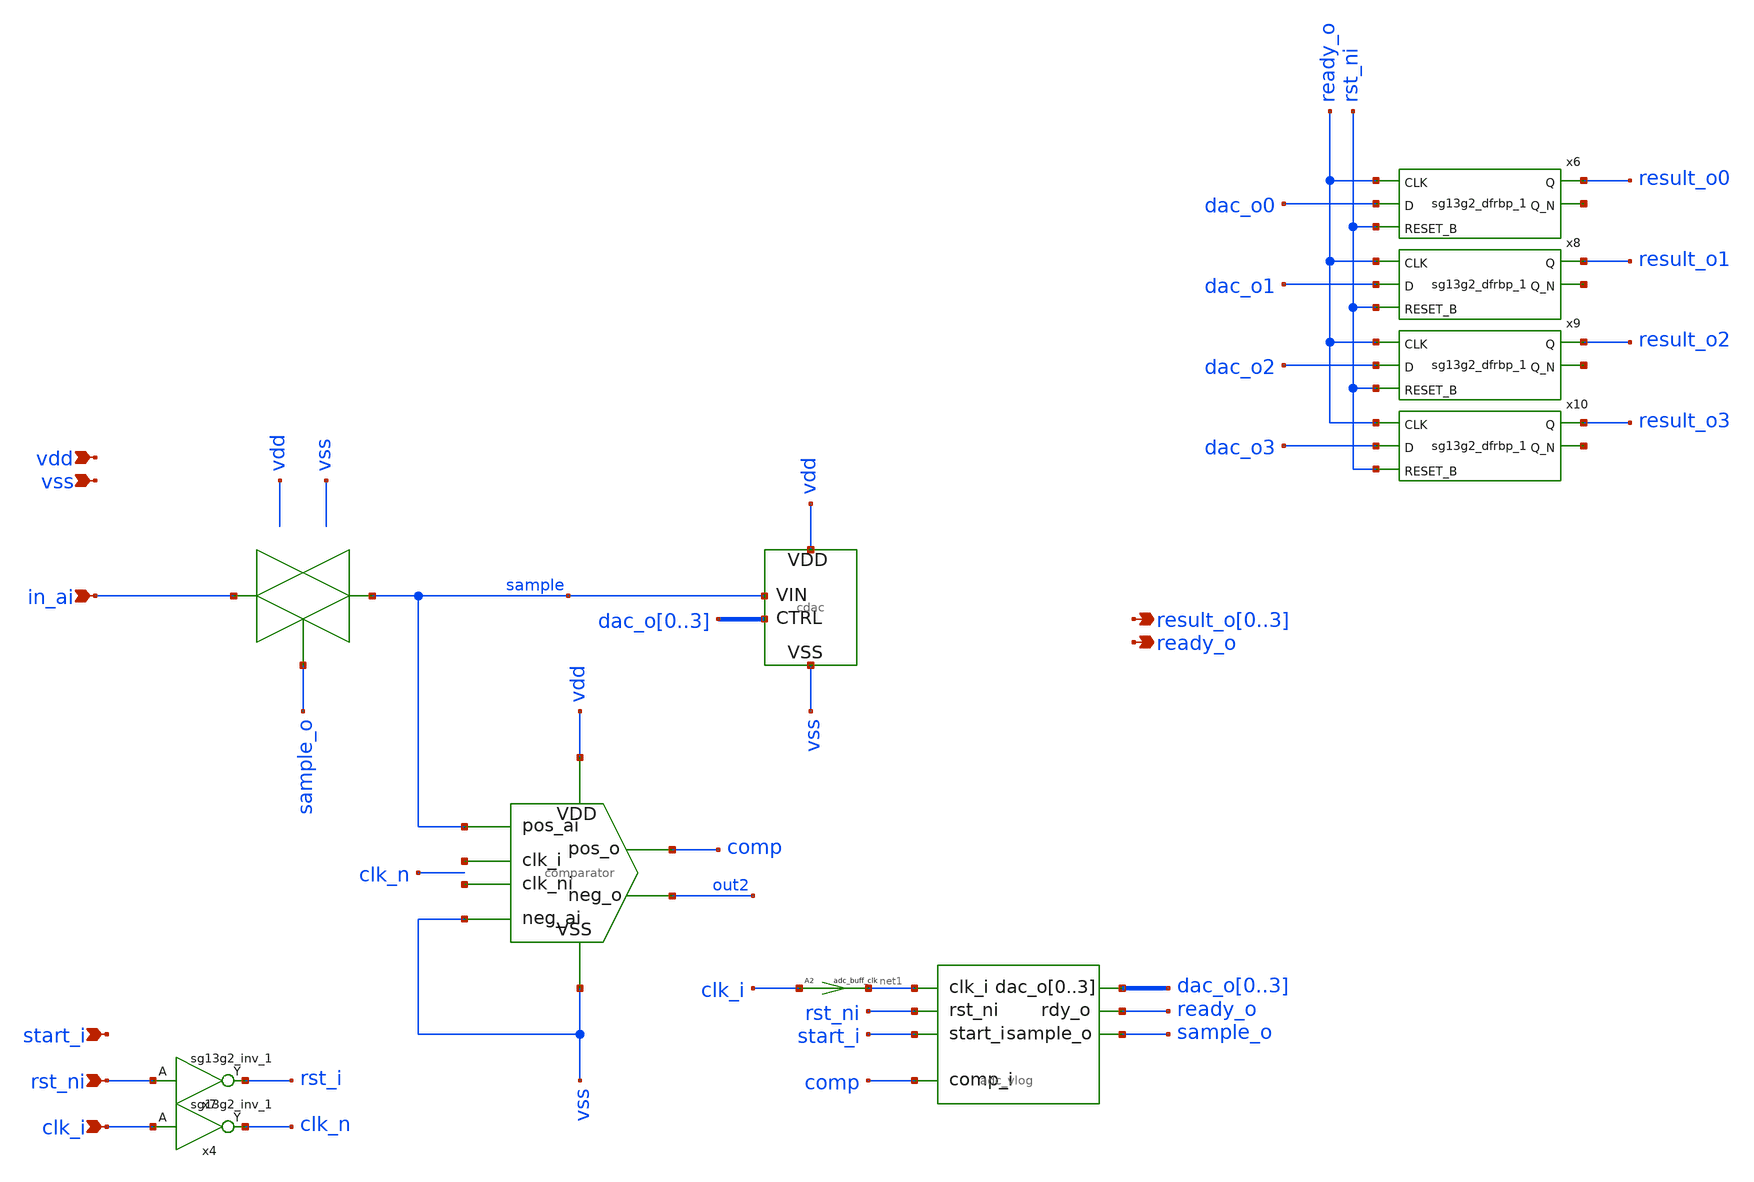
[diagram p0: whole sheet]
** sch_path: designs/basic/adc.sch
* IHP-GmbH/IHP-Open-PDK/ihp-sg13g2/libs.tech/xschem/sg13g2_stdcells/sg13g2_inv_2.sch:
* Copyright 2023 IHP PDK Authors
* Licensed under the Apache License, Version 2.0 (the "License");
**.subckt adc in_ai clk_i vss vdd rst_ni start_i ready_o result_o0,result_o1,result_o2,result_o3
*.ipin in_ai
*.ipin clk_i
*.ipin vss
*.ipin vdd
*.ipin rst_ni
*.ipin start_i
*.opin ready_o
*.opin result_o0,result_o1,result_o2,result_o3
x2 net2 sample vss out2 comp vss vdd net3 comparator
x3 sample dac_o0 dac_o1 dac_o2 dac_o3 dac_o0 dac_o1 dac_o2 dac_o3 vss vdd cdac
x4 clk_n clk_i VDD VSS sg13g2_inv_1
A2 [ clk_i ] [ net1 ] adc_buff_clk
x7 rst_i rst_ni VDD VSS sg13g2_inv_1
A1 [ net1 start_i rst_ni comp ] [ ready_o sample_o dac_o0 dac_o1 dac_o2 dac_o3 ] adc
x6 result_o0 net4 ready_o dac_o0 rst_ni VDD VSS sg13g2_dfrbp_1
x8 result_o1 net5 ready_o dac_o1 rst_ni VDD VSS sg13g2_dfrbp_1
x9 result_o2 net6 ready_o dac_o2 rst_ni VDD VSS sg13g2_dfrbp_1
x10 result_o3 net7 ready_o dac_o3 rst_ni VDD VSS sg13g2_dfrbp_1
**.ends

* expanding   symbol:  /workspaces/ngspice_cosim_inv/designs/comparator/comparator.sym # of pins=8
** sym_path: designs/comparator_dt/comparator.sym
** sch_path: designs/comparator_dt/comparator.sch
.subckt comparator clk_i pos_ai neg_ai neg_o pos_o VSS VDD clk_ni
*.ipin pos_ai
*.ipin neg_ai
*.ipin VSS
*.ipin VDD
*.opin neg_o
*.opin pos_o
*.ipin clk_i
*.ipin clk_ni
XM12 neg_buf clk_i VDD VDD sg13_lv_pmos w=1.0u l=0.13u ng=1 m=1 mm_ok=1
XM13 pos_buf clk_i VDD VDD sg13_lv_pmos w=1.0u l=0.13u ng=1 m=1 mm_ok=1
XM14 net1 pos_ai neg_buf VSS sg13_lv_nmos w=1.0u l=0.13u ng=1 m=1 mm_ok=1
XM15 net1 neg_ai pos_buf VSS sg13_lv_nmos w=1.0u l=0.13u ng=1 m=1 mm_ok=1
XM16 VSS clk_i net1 VSS sg13_lv_nmos w=1.0u l=0.13u ng=1 m=1 mm_ok=1
XM17 net2 clk_ni VDD VDD sg13_lv_pmos w=2.0u l=0.13u ng=2 m=1 mm_ok=1
XM18 pos_o neg_o net2 VDD sg13_lv_pmos w=2.0u l=0.13u ng=2 m=1 mm_ok=1
XM19 neg_o pos_o net2 VDD sg13_lv_pmos w=2.0u l=0.13u ng=2 m=1 mm_ok=1
XM20 VSS neg_buf pos_o VSS sg13_lv_nmos w=1.0u l=0.13u ng=1 m=1 mm_ok=1
XM21 VSS neg_o pos_o VSS sg13_lv_nmos w=1.0u l=0.13u ng=1 m=1 mm_ok=1
XM22 VSS pos_o neg_o VSS sg13_lv_nmos w=1.0u l=0.13u ng=1 m=1 mm_ok=1
XM23 VSS pos_buf neg_o VSS sg13_lv_nmos w=1.0u l=0.13u ng=1 m=1 mm_ok=1
XC1 neg_buf VSS cap_cmim w=1.41e-5 l=1.41e-5 m=1 mm_ok=1
XC2 pos_buf VSS cap_cmim w=1.41e-5 l=1.41e-5 m=1 mm_ok=1
.ends


* expanding   symbol:  /workspaces/ngspice_cosim_inv/designs/cdac/cdac.sym # of pins=4
** sym_path: designs/cdac/cdac.sym
** sch_path: designs/cdac/cdac.sch
.subckt cdac VIN CTRL0 CTRL1 CTRL2 CTRL3 CTRL4 CTRL5 CTRL6 CTRL7 VSS VDD
*.ipin VIN
*.ipin CTRL0,CTRL1,CTRL2,CTRL3,CTRL4,CTRL5,CTRL6,CTRL7
*.ipin VSS
*.ipin VDD
XC2 VIN l1 cap_cmim w=7.297e-5 l=7.298e-5 m=1 mm_ok=1
XC3 VIN l2 cap_cmim w=5.158e-5 l=5.159e-5 m=1 mm_ok=1
XC4 VIN l3 cap_cmim w=3.646e-5 l=3.646e-5 m=1 mm_ok=1
XC5 VIN VSS cap_cmim w=6.402e-6 l=6.402e-6 m=1 mm_ok=1
x1 l1 CTRL0 VDD VSS sg13g2_inv_2
x2 l2 CTRL1 VDD VSS sg13g2_inv_2
x3 l3 CTRL2 VDD VSS sg13g2_inv_2
x4 l4 CTRL3 VDD VSS sg13g2_inv_2
XC6 VIN l4 cap_cmim w=2.577e-5 l=2.577e-5 m=1 mm_ok=1
XC7 VIN l5 cap_cmim w=1.820e-5 l=1.820e-5 m=1 mm_ok=1
XC8 VIN l6 cap_cmim w=1.286e-5 l=1.286e-5 m=1 mm_ok=1
XC9 VIN l7 cap_cmim w=9.077e-6 l=9.077e-6 m=1 mm_ok=1
x5 l5 CTRL4 VDD VSS sg13g2_inv_2
x6 l6 CTRL5 VDD VSS sg13g2_inv_2
x7 l7 CTRL6 VDD VSS sg13g2_inv_2
x8 l8 CTRL7 VDD VSS sg13g2_inv_2
XC1 VIN l8 cap_cmim w=6.402e-6 l=6.402e-6 m=1 mm_ok=1
.ends


* expanding   symbol:  sg13g2_stdcells/sg13g2_inv_1.sym # of pins=2
** sym_path: sg13g2_stdcells/sg13g2_inv_1.sym
** sch_path: sg13g2_stdcells/sg13g2_inv_1.sch
.subckt sg13g2_inv_1 Y A VDD VSS
*.opin Y
*.ipin A
*.iopin VDD
*.iopin VSS
XM1 Y A VSS VSS sg13_lv_nmos w=740.00n l=130.00n ng=1 m=1 mm_ok=1
XM2 Y A VDD VDD sg13_lv_pmos w=1.12u l=130.00n ng=1 m=1 mm_ok=1
.ends


* expanding   symbol:  sg13g2_stdcells/sg13g2_dfrbp_1.sym # of pins=5
** sym_path: sg13g2_stdcells/sg13g2_dfrbp_1.sym
** sch_path: sg13g2_stdcells/sg13g2_dfrbp_1.sch
.subckt sg13g2_dfrbp_1 Q Q_N CLK D RESET_B VDD VSS
*.ipin D
*.ipin RESET_B
*.ipin CLK
*.opin Q
*.opin Q_N
*.iopin VDD
*.iopin VSS
XM1 Db D net10 VSS sg13_lv_nmos w=420.00n l=130.00n ng=1 m=1 mm_ok=1
XM2 net10 RESET_B VSS VSS sg13_lv_nmos w=420.00n l=130.00n ng=1 m=1 mm_ok=1
XM3 net1 clkneg net9 VSS sg13_lv_nmos w=420.00n l=130.00n ng=1 m=1 mm_ok=1
XM4 net9 net1 VSS VSS sg13_lv_nmos w=420.00n l=130.00n ng=1 m=1 mm_ok=1
XM5 net1 net1 net5 VSS sg13_lv_nmos w=420.00n l=130.00n ng=1 m=1 mm_ok=1
XM6 net5 RESET_B VSS VSS sg13_lv_nmos w=420.00n l=130.00n ng=1 m=1 mm_ok=1
XM7 Q_N net1 VSS VSS sg13_lv_nmos w=740.00n l=130.00n ng=1 m=1 mm_ok=1
XM8 net2 net1 VSS VSS sg13_lv_nmos w=740.00n l=130.00n ng=1 m=1 mm_ok=1
XM9 Q net2 VSS VSS sg13_lv_nmos w=740.00n l=130.00n ng=1 m=1 mm_ok=1
XM10 clkneg CLK VSS VSS sg13_lv_nmos w=740.00n l=130.00n ng=1 m=1 mm_ok=1
XM11 clkpos clkneg VSS VSS sg13_lv_nmos w=740.00n l=130.00n ng=1 m=1 mm_ok=1
XM12 Db clkneg net3 VSS sg13_lv_nmos w=420.00n l=130.00n ng=1 m=1 mm_ok=1
XM13 net3 clkpos net8 VSS sg13_lv_nmos w=420.00n l=130.00n ng=1 m=1 mm_ok=1
XM14 net8 net3 net4 VSS sg13_lv_nmos w=420.00n l=130.00n ng=1 m=1 mm_ok=1
XM15 net4 RESET_B VSS VSS sg13_lv_nmos w=420.00n l=130.00n ng=1 m=1 mm_ok=1
XM16 net3 net3 VSS VSS sg13_lv_nmos w=740.00n l=130.00n ng=1 m=1 mm_ok=1
XM17 net3 clkpos net1 VSS sg13_lv_nmos w=740.00n l=130.00n ng=1 m=1 mm_ok=1
XM18 Db RESET_B VDD VDD sg13_lv_pmos w=420.00n l=130.00n ng=1 m=1 mm_ok=1
XM19 Db D VDD VDD sg13_lv_pmos w=420.00n l=130.00n ng=1 m=1 mm_ok=1
XM20 net7 net1 VDD VDD sg13_lv_pmos w=420.00n l=130.00n ng=1 m=1 mm_ok=1
XM21 net1 clkpos net7 VDD sg13_lv_pmos w=420.00n l=130.00n ng=1 m=1 mm_ok=1
XM22 net1 net1 VDD VDD sg13_lv_pmos w=420.00n l=130.00n ng=1 m=1 mm_ok=1
XM23 net1 RESET_B VDD VDD sg13_lv_pmos w=420.00n l=130.00n ng=1 m=1 mm_ok=1
XM24 Q_N net1 VDD VDD sg13_lv_pmos w=1.12u l=130.00n ng=1 m=1 mm_ok=1
XM25 net2 net1 VDD VDD sg13_lv_pmos w=1.12u l=130.00n ng=1 m=1 mm_ok=1
XM26 Q net2 VDD VDD sg13_lv_pmos w=1.12u l=130.00n ng=1 m=1 mm_ok=1
XM27 clkneg CLK VDD VDD sg13_lv_pmos w=1.12u l=130.00n ng=1 m=1 mm_ok=1
XM28 clkpos clkneg VDD VDD sg13_lv_pmos w=1.12u l=130.00n ng=1 m=1 mm_ok=1
XM29 Db clkpos net3 VDD sg13_lv_pmos w=420.00n l=130.00n ng=1 m=1 mm_ok=1
XM30 net6 net3 VDD VDD sg13_lv_pmos w=420.00n l=130.00n ng=1 m=1 mm_ok=1
XM31 net3 clkneg net6 VDD sg13_lv_pmos w=420.00n l=130.00n ng=1 m=1 mm_ok=1
XM32 net3 RESET_B VDD VDD sg13_lv_pmos w=420.00n l=130.00n ng=1 m=1 mm_ok=1
XM33 net3 net3 VDD VDD sg13_lv_pmos w=1.000u l=130.00n ng=1 m=1 mm_ok=1
XM34 net3 clkneg net1 VDD sg13_lv_pmos w=1.000u l=130.00n ng=1 m=1 mm_ok=1
.ends


* expanding   symbol:  sg13g2_stdcells/sg13g2_inv_2.sym # of pins=2
** sym_path: sg13g2_stdcells/sg13g2_inv_2.sym
** sch_path: sg13g2_stdcells/sg13g2_inv_2.sch
.subckt sg13g2_inv_2 Y A VDD VSS
*.opin Y
*.ipin A
*.iopin VDD
*.iopin VSS
XM1 Y A VSS VSS sg13_lv_nmos w=1.48u l=130.00n ng=2 m=1 mm_ok=1
XM2 Y A VDD VDD sg13_lv_pmos w=2.24u l=130.00n ng=2 m=1 mm_ok=1
.ends

**** begin user architecture code
.model adc d_cosim simulation="ivlng" sim_args=["adc"]
**** end user architecture code
.end
